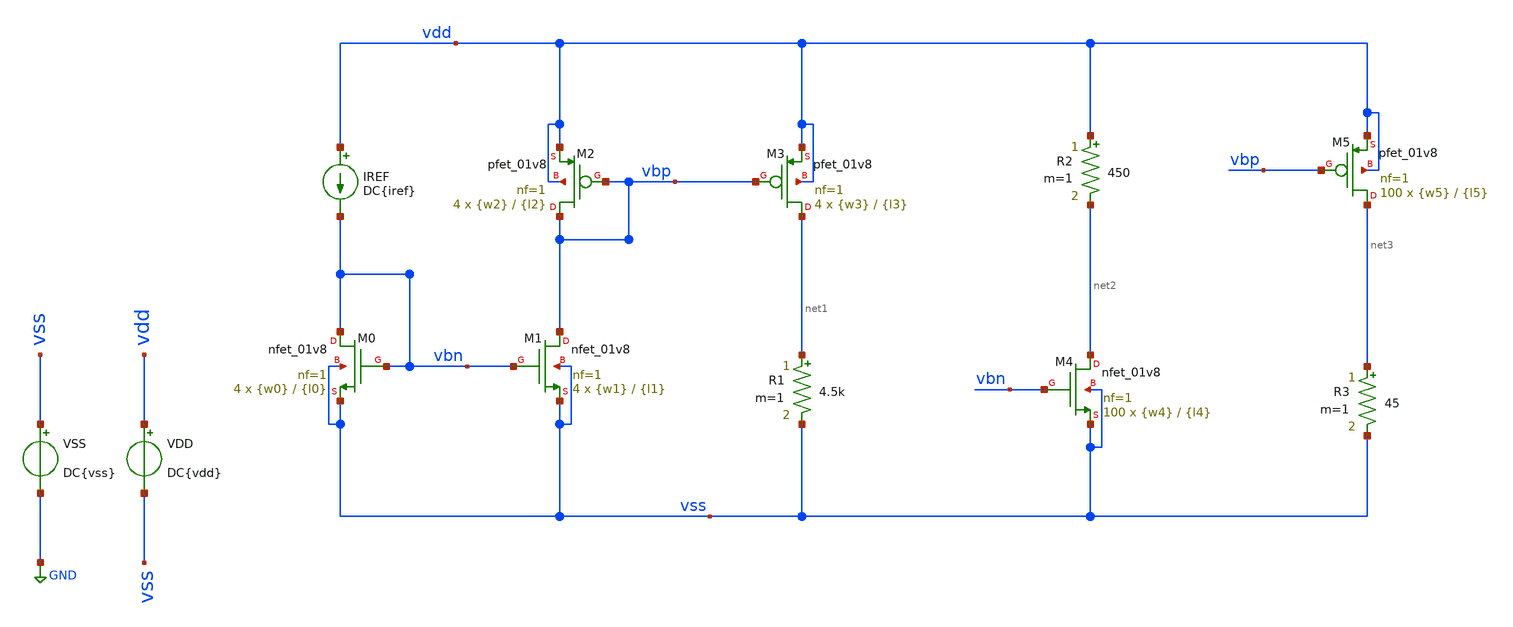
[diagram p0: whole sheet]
** sch_path: Tp2/Mis Simulaciones/tp2_4.sch
**.subckt tp2_4
XM0 vbn vbn vss vss sky130_fd_pr__nfet_01v8 L={l0} W={w0} nf=1 ad='int((nf+1)/2) * W/nf * 0.29' as='int((nf+2)/2) * W/nf * 0.29'
+ pd='2*int((nf+1)/2) * (W/nf + 0.29)' ps='2*int((nf+2)/2) * (W/nf + 0.29)' nrd='0.29 / W' nrs='0.29 / W'
+ sa=0 sb=0 sd=0 mult=4 m=4
XM1 vbp vbn vss vss sky130_fd_pr__nfet_01v8 L={l1} W={w1} nf=1 ad='int((nf+1)/2) * W/nf * 0.29' as='int((nf+2)/2) * W/nf * 0.29'
+ pd='2*int((nf+1)/2) * (W/nf + 0.29)' ps='2*int((nf+2)/2) * (W/nf + 0.29)' nrd='0.29 / W' nrs='0.29 / W'
+ sa=0 sb=0 sd=0 mult=4 m=4
IREF vdd vbn DC{iref}
VSS vss GND DC{vss}
VDD vdd vss DC{vdd}
XM2 vbp vbp vdd vdd sky130_fd_pr__pfet_01v8 L={l2} W={w2} nf=1 ad='int((nf+1)/2) * W/nf * 0.29' as='int((nf+2)/2) * W/nf * 0.29'
+ pd='2*int((nf+1)/2) * (W/nf + 0.29)' ps='2*int((nf+2)/2) * (W/nf + 0.29)' nrd='0.29 / W' nrs='0.29 / W'
+ sa=0 sb=0 sd=0 mult=4 m=4
XM3 net1 vbp vdd vdd sky130_fd_pr__pfet_01v8 L={l3} W={w3} nf=1 ad='int((nf+1)/2) * W/nf * 0.29' as='int((nf+2)/2) * W/nf * 0.29'
+ pd='2*int((nf+1)/2) * (W/nf + 0.29)' ps='2*int((nf+2)/2) * (W/nf + 0.29)' nrd='0.29 / W' nrs='0.29 / W'
+ sa=0 sb=0 sd=0 mult=4 m=4
XM4 net2 vbn vss vss sky130_fd_pr__nfet_01v8 L={l4} W={w4} nf=1 ad='int((nf+1)/2) * W/nf * 0.29' as='int((nf+2)/2) * W/nf * 0.29'
+ pd='2*int((nf+1)/2) * (W/nf + 0.29)' ps='2*int((nf+2)/2) * (W/nf + 0.29)' nrd='0.29 / W' nrs='0.29 / W'
+ sa=0 sb=0 sd=0 mult=100 m=100
XM5 net3 vbp vdd vdd sky130_fd_pr__pfet_01v8 L={l5} W={w5} nf=1 ad='int((nf+1)/2) * W/nf * 0.29' as='int((nf+2)/2) * W/nf * 0.29'
+ pd='2*int((nf+1)/2) * (W/nf + 0.29)' ps='2*int((nf+2)/2) * (W/nf + 0.29)' nrd='0.29 / W' nrs='0.29 / W'
+ sa=0 sb=0 sd=0 mult=100 m=100
R1 net1 vss 4.5k m=1
R2 vdd net2 450 m=1
R3 net3 vss 45 m=1
**** begin user architecture code



* Parameters
.param vdd = 1.8
.param vss = 0.0
.param iref = 200u
.param w0 = 11.25
.param l0 = 0.15
.param w1 = w0
.param l1 = 0.15
.param w2 = 22.5
.param l2 = 0.3
.param w3 = w2
.param l3 = 0.3
.param w4 = 4.5
.param l4 = 0.15
.param w5 = 90
.param l5 = 0.3
.options TEMPS = 27.0

* Models
.lib ~/skywater/skywater-pdk/libraries/sky130_fd_pr_ngspice/latest/models/corners/sky130.lib TT

* Data to save
.save all  @M.XM0.msky130_fd_pr__nfet_01v8[id]  @M.XM0.msky130_fd_pr__nfet_01v8[vth]  @M.XM0.msky130_fd_pr__nfet_01v8[vdsat]  @M.XM0.msky130_fd_pr__nfet_01v8[gm]  @M.XM0.msky130_fd_pr__nfet_01v8[vds]  @M.XM0.msky130_fd_pr__nfet_01v8[vgs]  @M.XM0.msky130_fd_pr__nfet_01v8[w]  @M.XM1.msky130_fd_pr__nfet_01v8[id]  @M.XM1.msky130_fd_pr__nfet_01v8[vth]  @M.XM1.msky130_fd_pr__nfet_01v8[vdsat]  @M.XM1.msky130_fd_pr__nfet_01v8[gm]  @M.XM1.msky130_fd_pr__nfet_01v8[vds]  @M.XM1.msky130_fd_pr__nfet_01v8[vgs]  @M.XM1.msky130_fd_pr__nfet_01v8[w]  @M.XM2.msky130_fd_pr__pfet_01v8[id]  @M.XM2.msky130_fd_pr__pfet_01v8[vth]  @M.XM2.msky130_fd_pr__pfet_01v8[vdsat]  @M.XM2.msky130_fd_pr__pfet_01v8[gm]  @M.XM2.msky130_fd_pr__pfet_01v8[vds]  @M.XM2.msky130_fd_pr__pfet_01v8[vgs]  @M.XM2.msky130_fd_pr__pfet_01v8[w]  @M.XM3.msky130_fd_pr__pfet_01v8[id]  @M.XM3.msky130_fd_pr__pfet_01v8[vth]  @M.XM3.msky130_fd_pr__pfet_01v8[vdsat]  @M.XM3.msky130_fd_pr__pfet_01v8[gm]  @M.XM3.msky130_fd_pr__pfet_01v8[vds]  @M.XM3.msky130_fd_pr__pfet_01v8[vgs]  @M.XM3.msky130_fd_pr__pfet_01v8[w]  @M.XM4.msky130_fd_pr__nfet_01v8[id]  @M.XM4.msky130_fd_pr__nfet_01v8[vth]  @M.XM4.msky130_fd_pr__nfet_01v8[vdsat]  @M.XM4.msky130_fd_pr__nfet_01v8[gm]  @M.XM4.msky130_fd_pr__nfet_01v8[vds]  @M.XM4.msky130_fd_pr__nfet_01v8[vgs]  @M.XM4.msky130_fd_pr__nfet_01v8[w]  @M.XM5.msky130_fd_pr__pfet_01v8[id]  @M.XM5.msky130_fd_pr__pfet_01v8[vth]  @M.XM5.msky130_fd_pr__pfet_01v8[vdsat]  @M.XM5.msky130_fd_pr__pfet_01v8[gm]  @M.XM5.msky130_fd_pr__pfet_01v8[vds]  @M.XM5.msky130_fd_pr__pfet_01v8[vgs]  @M.XM5.msky130_fd_pr__pfet_01v8[w]

* Simulation
.control
  *let wi = 1.5
  *let wf = 4.5
  *let wstep = 0.15

  *dowhile wi <= wf
    *print @M.XM0.msky130_fd_pr__nfet_01v8[w]
    *alter @M.XM0.msky130_fd_pr__nfet_01v8[w] = wi
    *alter @M.XM1.msky130_fd_pr__nfet_01v8[w] = wi
    *let wi = wi + wstep
    *op
    *print @M.XM0.msky130_fd_pr__nfet_01v8[w]
    *print @M.XM0.msky130_fd_pr__nfet_01v8[id]
    *print @M.XM0.msky130_fd_pr__nfet_01v8[vds]
    *print @M.XM0.msky130_fd_pr__nfet_01v8[vgs]
    *print @M.XM1.msky130_fd_pr__nfet_01v8[w]
    *print @M.XM1.msky130_fd_pr__nfet_01v8[id]
    *print @M.XM1.msky130_fd_pr__nfet_01v8[vds]
    *print @M.XM1.msky130_fd_pr__nfet_01v8[vgs]
    *print @M.XM2.msky130_fd_pr__pfet_01v8[w]
    *print @M.XM2.msky130_fd_pr__pfet_01v8[id]
    *print @M.XM2.msky130_fd_pr__pfet_01v8[vds]
    *print @M.XM2.msky130_fd_pr__pfet_01v8[vgs]
    *print @M.XM3.msky130_fd_pr__pfet_01v8[w]
    *print @M.XM3.msky130_fd_pr__pfet_01v8[id]
    *print @M.XM3.msky130_fd_pr__pfet_01v8[vds]
    *print @M.XM3.msky130_fd_pr__pfet_01v8[vgs]
    *print @M.XM4.msky130_fd_pr__nfet_01v8[w]
    *print @M.XM4.msky130_fd_pr__nfet_01v8[id]
    *print @M.XM4.msky130_fd_pr__nfet_01v8[vds]
    *print @M.XM4.msky130_fd_pr__nfet_01v8[vgs]
    *print @M.XM5.msky130_fd_pr__pfet_01v8[w]
    *print @M.XM5.msky130_fd_pr__pfet_01v8[id]
    *print @M.XM5.msky130_fd_pr__pfet_01v8[vds]
    *print @M.XM5.msky130_fd_pr__pfet_01v8[vgs]
    *save all
  *end
  *write tp2_4.raw

  unset filetype
  op
  save all
  write tp2_4.raw

.endc

.end


**** end user architecture code
**.ends
.GLOBAL GND
.end
